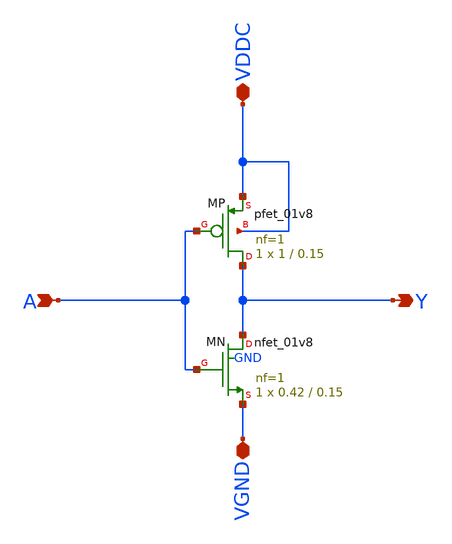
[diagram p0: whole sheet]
** sch_path: designs/bgr_ldo/layout/ro_inv/ro_inv.sch
**.subckt ro_inv VDDC VGND A Y
*.iopin VDDC
*.iopin VGND
*.ipin A
*.opin Y
XMN Y A VGND GND sky130_fd_pr__nfet_01v8 L=0.15 W=0.42 nf=1 ad='int((1 + 1)/2) * 0.42 / 1 * 0.29' as='int((1 + 2)/2) * 0.42 / 1 * 0.29'
+ pd='2*int((1 + 1)/2) * (0.42 / 1 + 0.29)' ps='2*int((1 + 2)/2) * (0.42 / 1 + 0.29)' nrd='0.29 / 0.42 '
+ nrs='0.29 / 0.42 ' sa=0 sb=0 sd=0 mult=1 m=1
XMP Y A VDDC VDDC sky130_fd_pr__pfet_01v8 L=0.15 W=1 nf=1 ad='int((1 + 1)/2) * 1 / 1 * 0.29' as='int((1 + 2)/2) * 1 / 1 * 0.29'
+ pd='2*int((1 + 1)/2) * (1 / 1 + 0.29)' ps='2*int((1 + 2)/2) * (1 / 1 + 0.29)' nrd='0.29 / 1 ' nrs='0.29 / 1 '
+ sa=0 sb=0 sd=0 mult=1 m=1
**.ends
.end
